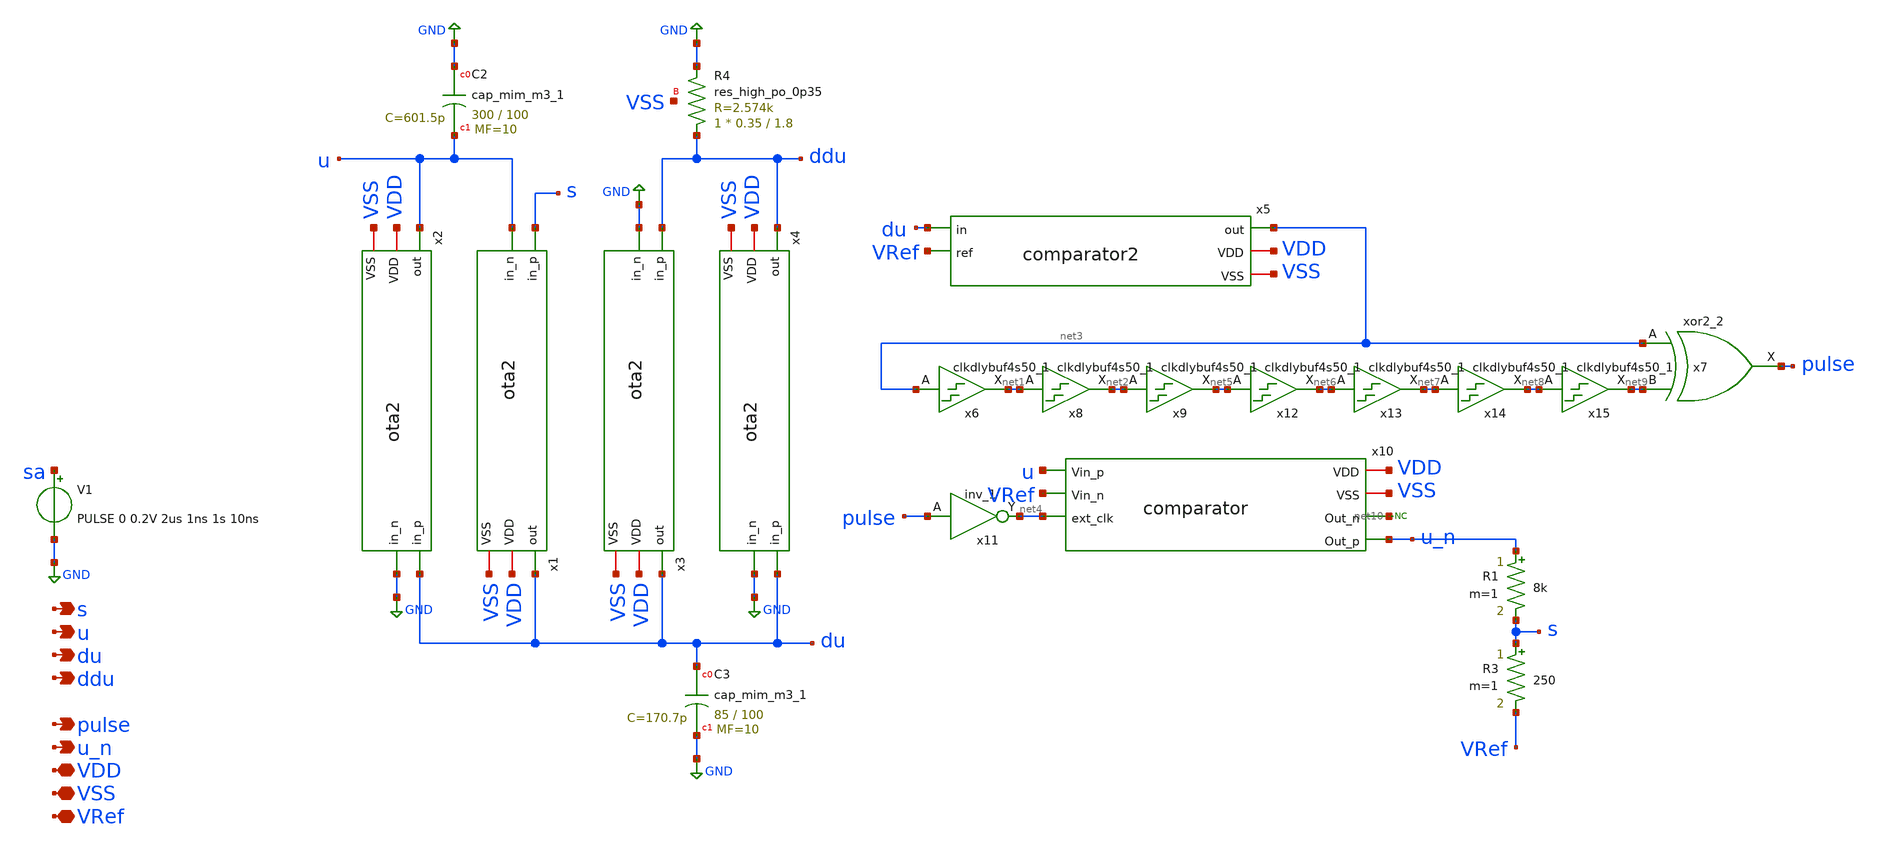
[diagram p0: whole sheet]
** sch_path: xschem/src/oscilator/oscilator.sch
**.subckt oscilator VDD s VSS VRef u du pulse u_n ddu
*.iopin VDD
*.opin s
*.iopin VSS
*.iopin VRef
*.opin u
*.opin du
*.opin pulse
*.opin u_n
*.opin ddu
x2 u du GND VDD VSS ota2
x1 du s u VDD VSS ota2
x3 du ddu GND VDD VSS ota2
x4 ddu du GND VDD VSS ota2
V1 sa GND PULSE 0 0.2V 2us 1ns 1s 10ns
x5 net3 VDD VSS du VRef comparator2
x6 net3 VSS VSS VDD VDD net1 sky130_fd_sc_hd__clkdlybuf4s50_1
x7 net3 net9 VSS VSS VDD VDD pulse sky130_fd_sc_hd__xor2_2
x8 net1 VSS VSS VDD VDD net2 sky130_fd_sc_hd__clkdlybuf4s50_1
x9 net2 VSS VSS VDD VDD net5 sky130_fd_sc_hd__clkdlybuf4s50_1
x10 VDD VSS u net10 VRef u_n net4 comparator
x11 pulse VSS VSS VDD VDD net4 sky130_fd_sc_hd__inv_1
* noconn #net10
R1 u_n s 8k m=1
R3 s VRef 250 m=1
x12 net5 VSS VSS VDD VDD net6 sky130_fd_sc_hd__clkdlybuf4s50_1
x13 net6 VSS VSS VDD VDD net7 sky130_fd_sc_hd__clkdlybuf4s50_1
x14 net7 VSS VSS VDD VDD net8 sky130_fd_sc_hd__clkdlybuf4s50_1
x15 net8 VSS VSS VDD VDD net9 sky130_fd_sc_hd__clkdlybuf4s50_1
XR4 ddu GND VSS sky130_fd_pr__res_high_po_0p35 L=1.8 mult=1 m=1
XC2 GND u sky130_fd_pr__cap_mim_m3_1 W=300 L=100 MF=10 m=10
XC3 du GND sky130_fd_pr__cap_mim_m3_1 W=85 L=100 MF=10 m=10
**.ends
.GLOBAL GND
.end
